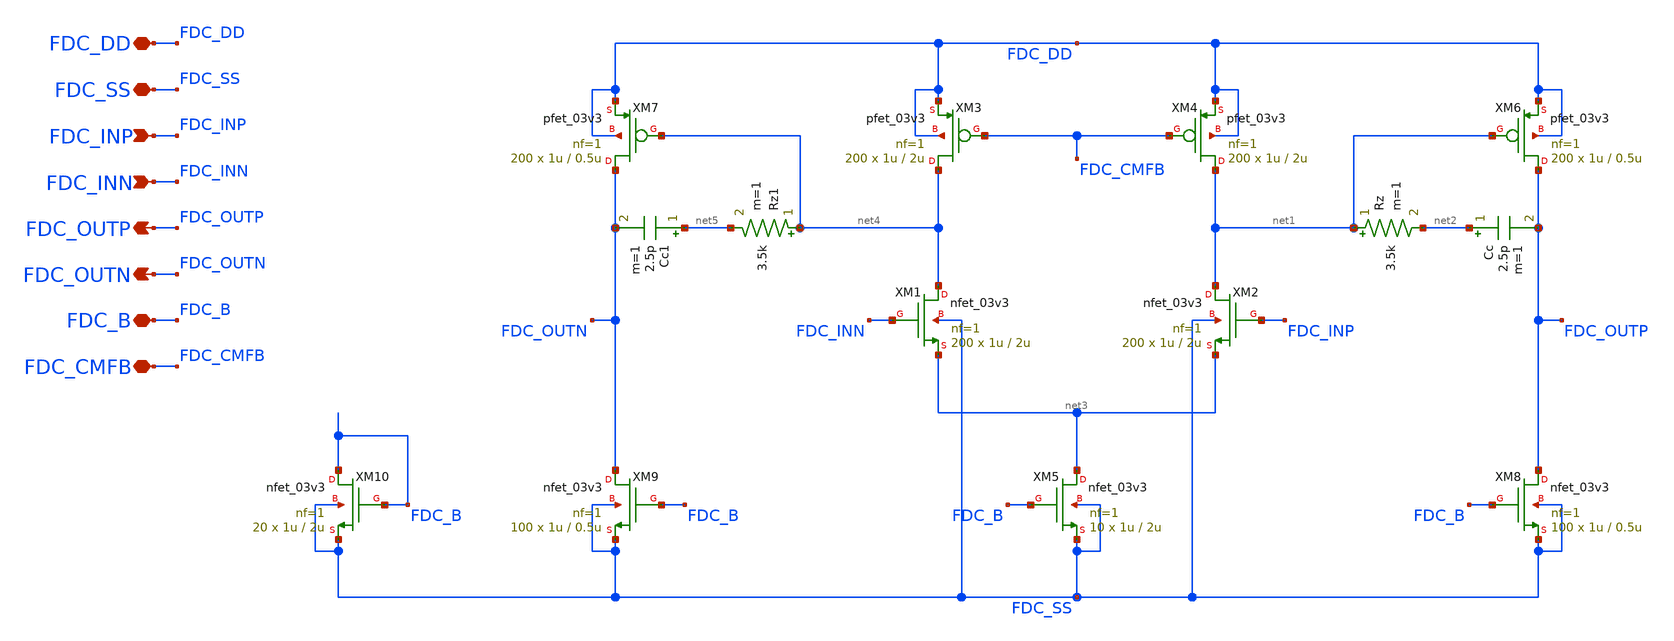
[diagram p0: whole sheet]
** sch_path: Design_Files/IC Design/Schematic/FD_OTA/FDC/FDC.sch
**.subckt FDC FDC_DD FDC_SS FDC_INP FDC_INN FDC_OUTP FDC_B FDC_OUTN FDC_CMFB
*.iopin FDC_DD
*.iopin FDC_SS
*.ipin FDC_INP
*.ipin FDC_INN
*.opin FDC_OUTP
*.iopin FDC_B
*.opin FDC_OUTN
*.iopin FDC_CMFB
XM3 net4 FDC_CMFB FDC_DD FDC_DD pfet_03v3 L=2u W=1u nf=1 ad='int((nf+1)/2) * W/nf * 0.18u' as='int((nf+2)/2) * W/nf * 0.18u'
+ pd='2*int((nf+1)/2) * (W/nf + 0.18u)' ps='2*int((nf+2)/2) * (W/nf + 0.18u)' nrd='0.18u / W' nrs='0.18u / W'
+ sa=0 sb=0 sd=0 m=200
XM8 FDC_OUTP FDC_B FDC_SS FDC_SS nfet_03v3 L=0.5u W=1u nf=1 ad='int((nf+1)/2) * W/nf * 0.18u' as='int((nf+2)/2) * W/nf * 0.18u'
+ pd='2*int((nf+1)/2) * (W/nf + 0.18u)' ps='2*int((nf+2)/2) * (W/nf + 0.18u)' nrd='0.18u / W' nrs='0.18u / W'
+ sa=0 sb=0 sd=0 m=100
Rz net1 net2 3.5k m=1
XM5 net3 FDC_B FDC_SS FDC_SS nfet_03v3 L=2u W=1u nf=1 ad='int((nf+1)/2) * W/nf * 0.18u' as='int((nf+2)/2) * W/nf * 0.18u'
+ pd='2*int((nf+1)/2) * (W/nf + 0.18u)' ps='2*int((nf+2)/2) * (W/nf + 0.18u)' nrd='0.18u / W' nrs='0.18u / W'
+ sa=0 sb=0 sd=0 m=10
XM6 FDC_OUTP net1 FDC_DD FDC_DD pfet_03v3 L=0.5u W=1u nf=1 ad='int((nf+1)/2) * W/nf * 0.18u' as='int((nf+2)/2) * W/nf * 0.18u'
+ pd='2*int((nf+1)/2) * (W/nf + 0.18u)' ps='2*int((nf+2)/2) * (W/nf + 0.18u)' nrd='0.18u / W' nrs='0.18u / W'
+ sa=0 sb=0 sd=0 m=200
XM10 FDC_B FDC_B FDC_SS FDC_SS nfet_03v3 L=2u W=1u nf=1 ad='int((nf+1)/2) * W/nf * 0.18u' as='int((nf+2)/2) * W/nf * 0.18u'
+ pd='2*int((nf+1)/2) * (W/nf + 0.18u)' ps='2*int((nf+2)/2) * (W/nf + 0.18u)' nrd='0.18u / W' nrs='0.18u / W'
+ sa=0 sb=0 sd=0 m=20
Cc net2 FDC_OUTP 2.5p m=1
XM9 FDC_OUTN FDC_B FDC_SS FDC_SS nfet_03v3 L=0.5u W=1u nf=1 ad='int((nf+1)/2) * W/nf * 0.18u' as='int((nf+2)/2) * W/nf * 0.18u'
+ pd='2*int((nf+1)/2) * (W/nf + 0.18u)' ps='2*int((nf+2)/2) * (W/nf + 0.18u)' nrd='0.18u / W' nrs='0.18u / W'
+ sa=0 sb=0 sd=0 m=100
Rz1 net4 net5 3.5k m=1
XM7 FDC_OUTN net4 FDC_DD FDC_DD pfet_03v3 L=0.5u W=1u nf=1 ad='int((nf+1)/2) * W/nf * 0.18u' as='int((nf+2)/2) * W/nf * 0.18u'
+ pd='2*int((nf+1)/2) * (W/nf + 0.18u)' ps='2*int((nf+2)/2) * (W/nf + 0.18u)' nrd='0.18u / W' nrs='0.18u / W'
+ sa=0 sb=0 sd=0 m=200
Cc1 net5 FDC_OUTN 2.5p m=1
XM4 net1 FDC_CMFB FDC_DD FDC_DD pfet_03v3 L=2u W=1u nf=1 ad='int((nf+1)/2) * W/nf * 0.18u' as='int((nf+2)/2) * W/nf * 0.18u'
+ pd='2*int((nf+1)/2) * (W/nf + 0.18u)' ps='2*int((nf+2)/2) * (W/nf + 0.18u)' nrd='0.18u / W' nrs='0.18u / W'
+ sa=0 sb=0 sd=0 m=200
XM1 net4 FDC_INN net3 FDC_SS nfet_03v3 L=2u W=1u nf=1 ad='int((nf+1)/2) * W/nf * 0.18u' as='int((nf+2)/2) * W/nf * 0.18u'
+ pd='2*int((nf+1)/2) * (W/nf + 0.18u)' ps='2*int((nf+2)/2) * (W/nf + 0.18u)' nrd='0.18u / W' nrs='0.18u / W'
+ sa=0 sb=0 sd=0 m=200
XM2 net1 FDC_INP net3 FDC_SS nfet_03v3 L=2u W=1u nf=1 ad='int((nf+1)/2) * W/nf * 0.18u' as='int((nf+2)/2) * W/nf * 0.18u'
+ pd='2*int((nf+1)/2) * (W/nf + 0.18u)' ps='2*int((nf+2)/2) * (W/nf + 0.18u)' nrd='0.18u / W' nrs='0.18u / W'
+ sa=0 sb=0 sd=0 m=200
**.ends
.end
